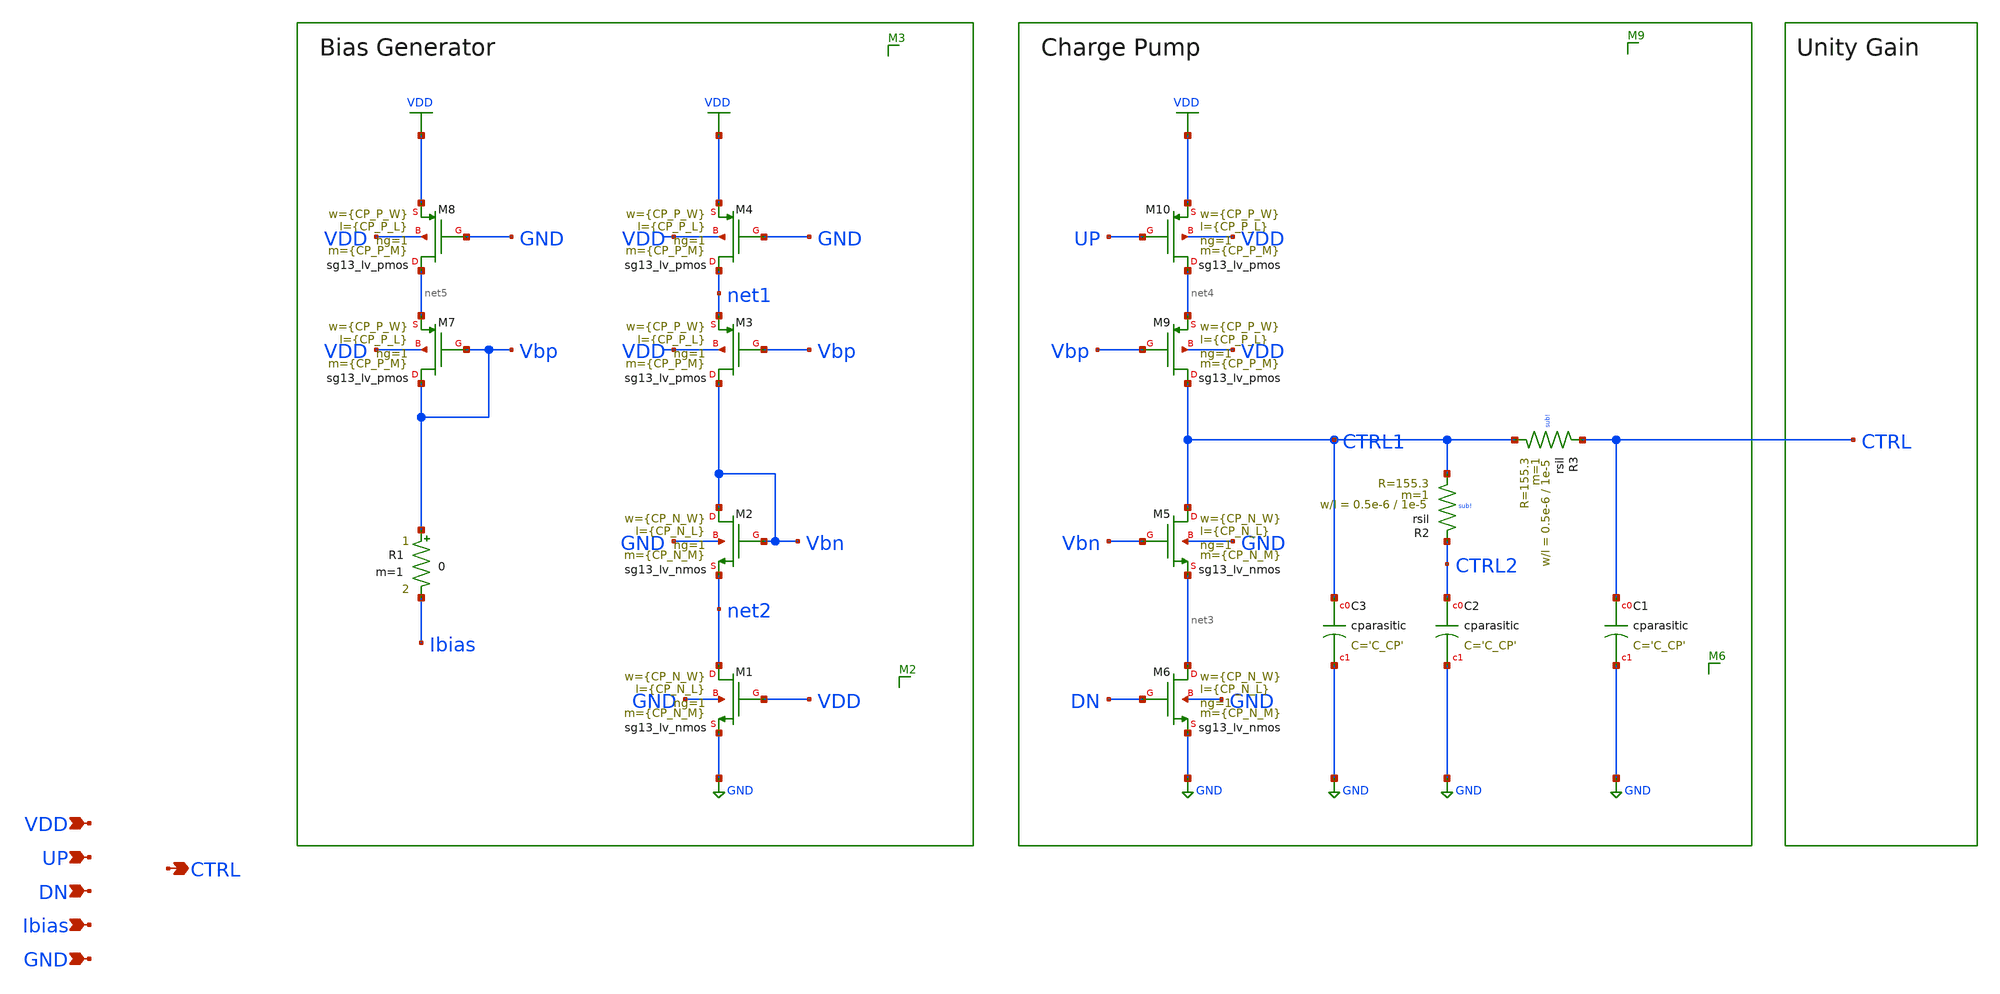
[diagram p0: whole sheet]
** sch_path: schematic/blocks/charge-pump/CP.sch
**.subckt CP CTRL UP VDD Ibias DN GND
*.opin CTRL
*.ipin UP
*.ipin VDD
*.ipin Ibias
*.ipin DN
*.ipin GND
XM2 Vbn Vbn net2 GND sg13_lv_nmos w={CP_N_W} l={CP_N_L} ng=1 m={CP_N_M} mm_ok=1
XM1 net2 VDD GND GND sg13_lv_nmos w={CP_N_W} l={CP_N_L} ng=1 m={CP_N_M} mm_ok=1
XM3 Vbn Vbp net1 VDD sg13_lv_pmos w={CP_P_W} l={CP_P_L} ng=1 m={CP_P_M} mm_ok=1
XM4 net1 GND VDD VDD sg13_lv_pmos w={CP_P_W} l={CP_P_L} ng=1 m={CP_P_M} mm_ok=1
XM7 Vbp Vbp net5 VDD sg13_lv_pmos w={CP_P_W} l={CP_P_L} ng=1 m={CP_P_M} mm_ok=1
XM8 net5 GND VDD VDD sg13_lv_pmos w={CP_P_W} l={CP_P_L} ng=1 m={CP_P_M} mm_ok=1
XM5 CTRL1 Vbn net3 GND sg13_lv_nmos w={CP_N_W} l={CP_N_L} ng=1 m={CP_N_M} mm_ok=1
XM6 net3 DN GND GND sg13_lv_nmos w={CP_N_W} l={CP_N_L} ng=1 m={CP_N_M} mm_ok=1
XM9 CTRL1 Vbp net4 VDD sg13_lv_pmos w={CP_P_W} l={CP_P_L} ng=1 m={CP_P_M} mm_ok=1
XM10 net4 UP VDD VDD sg13_lv_pmos w={CP_P_W} l={CP_P_L} ng=1 m={CP_P_M} mm_ok=1
XC1 CTRL GND cparasitic C='C_CP'
XR3 CTRL CTRL1 sub! rsil w=0.5e-6 l=1e-5 m=1 mm_ok=1
XC2 CTRL2 GND cparasitic C='C_CP'
XR2 CTRL2 CTRL1 sub! rsil w=0.5e-6 l=1e-5 m=1 mm_ok=1
XC3 CTRL1 GND cparasitic C='C_CP'
R1 Vbp Ibias 0 m=1
**.ends
.GLOBAL GND
.GLOBAL VDD
.end
